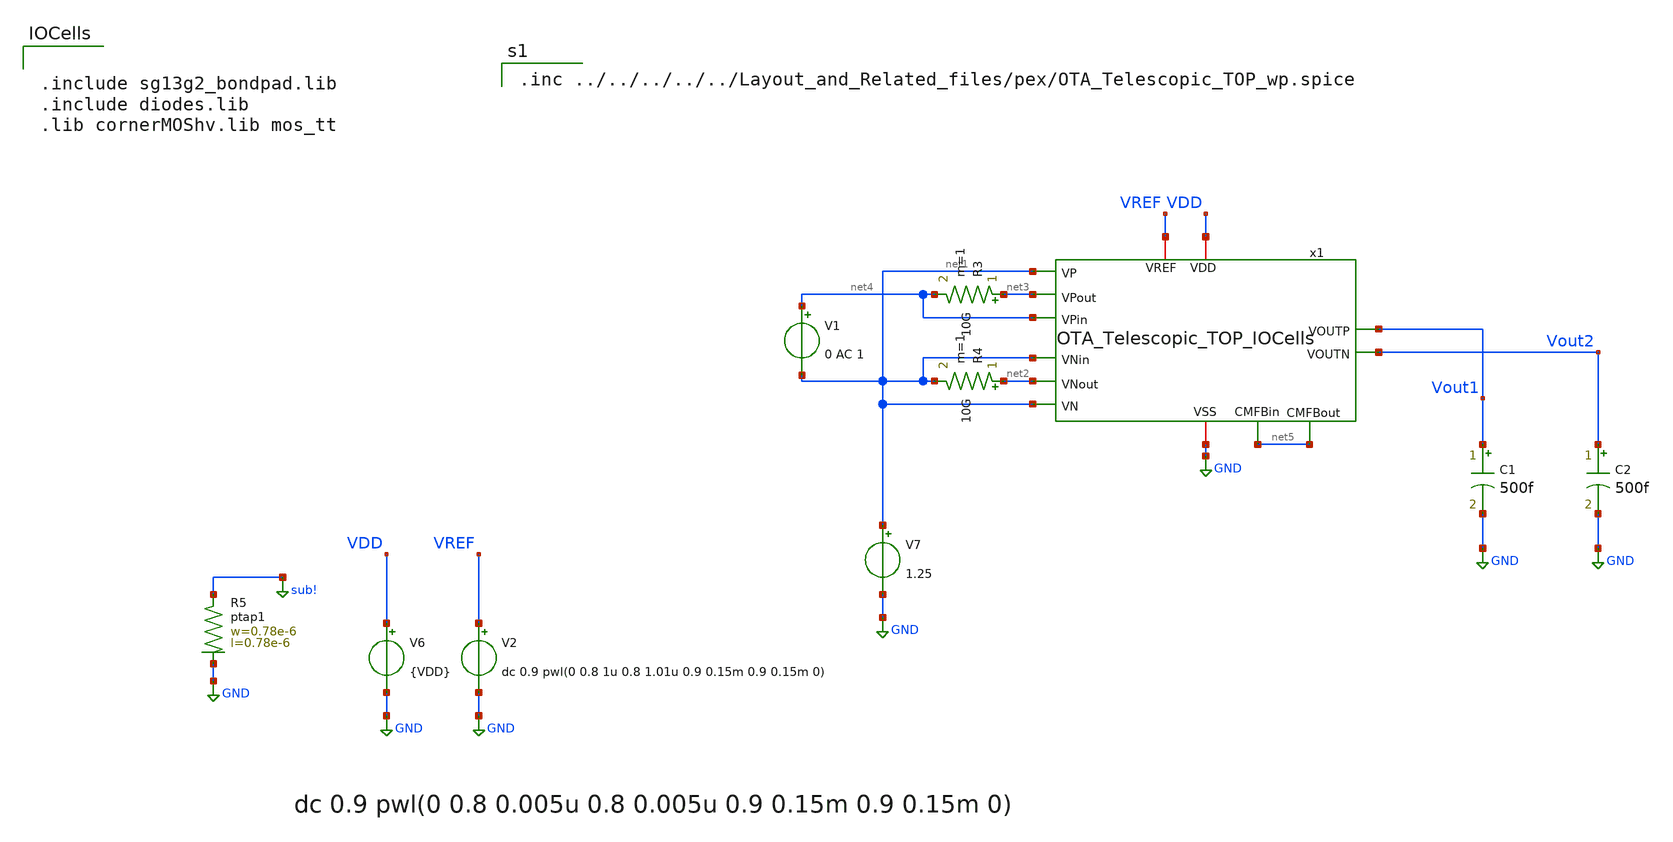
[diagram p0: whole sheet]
** sch_path: OTA_Telescopic/AutoTestbench/tb/OTA_Telescopic_TOP_TB_OL_io.sch
**.subckt OTA_Telescopic_TOP_TB_OL_io
V7 net1 GND 1.25
C1 Vout1 GND 500f m=1
C2 Vout2 GND 500f m=1
V6 VDD GND {VDD}
R3 net3 net4 10G m=1
R4 net2 net1 10G m=1
V1 net4 net1 0 AC 1
V2 VREF GND dc 0.9 pwl(0 0.8 1u 0.8 1.01u 0.9 0.15m 0.9 0.15m 0)
XR5 sub! GND ptap1 R=262.8 w=0.78e-6 l=0.78e-6
x1 VDD GND net3 net1 net4 Vout2 Vout1 net1 net2 net1 VREF net5 net5 OTA_Telescopic_TOP_IOCells
**** begin user architecture code


** opencircuitdesign pdks install
.lib cornerMOSlv.lib mos_$PROCESS
.lib cornerRES.lib res_typ
.lib cornerCAP.lib cap_typ
.temp $TEMP




*.nodeset v(Vout1)=0.9 v(Vout2)=0.9
.param VDD=$VDD
.control
save Vout1 Vout2
 set color0 = white

* AC simulation
ac dec 10 1 1T
let Av = db((v(Vout2)-v(Vout1)))
meas ac Ao FIND Av WHEN frequency=10
let ABW = Ao-3
meas ac BW WHEN Av=ABW
meas ac UGBW WHEN Av=0
let phase_vec = 180/pi*cph(v(Vout2)-v(Vout1))

* Phase margin (PM)
meas ac phase FIND phase_vec WHEN frequency=UGBW
let PM = phase+180
print PM

* Gain margin (GM)
meas ac freq180 FIND frequency WHEN phase_vec=-180
meas ac gain FIND Av WHEN frequency=freq180
let GM = 0-gain

*BW in 7 dB
meas ac UGBW7dB WHEN Av=7
meas ac UGBW4dB WHEN Av=4

print GM
plot Av
plot phase_vec

plot db(v(x1.Vo1)-v(x1.Vo2))

write AC_OL.raw

wrdata AvOL.txt Av
wrdata PhaseOL.txt phase_vec

let Ao_ = Ao
let UGBW_ = UGBW

echo PM $&PM > results.txt
echo Ao $&Ao_ >> results.txt
echo UGBW $&UGBW_ >> results.txt


.endc




.include sg13g2_bondpad.lib
.include diodes.lib
.lib cornerMOShv.lib mos_tt



.inc ../../../../../Layout_and_Related_files/pex/OTA_Telescopic_TOP_wp.spice

**** end user architecture code
**.ends
.GLOBAL GND
.GLOBAL sub!
.end
